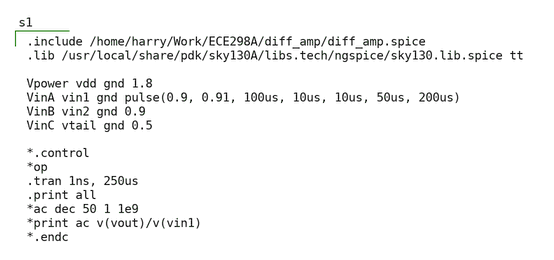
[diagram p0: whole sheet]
** sch_path: magic_xschem_ngspice/Magic_sim.sch
**.subckt Magic_sim
**** begin user architecture code

.include /home/harry/Work/ECE298A/diff_amp/diff_amp.spice
.lib /usr/local/share/pdk/sky130A/libs.tech/ngspice/sky130.lib.spice tt

Vpower vdd gnd 1.8
VinA vin1 gnd pulse(0.9, 0.91, 100us, 10us, 10us, 50us, 200us)
VinB vin2 gnd 0.9
VinC vtail gnd 0.5

*.control
*op
.tran 1ns, 250us
.print all
*ac dec 50 1 1e9
*print ac v(vout)/v(vin1)
*.endc

**** end user architecture code
**.ends
.end
